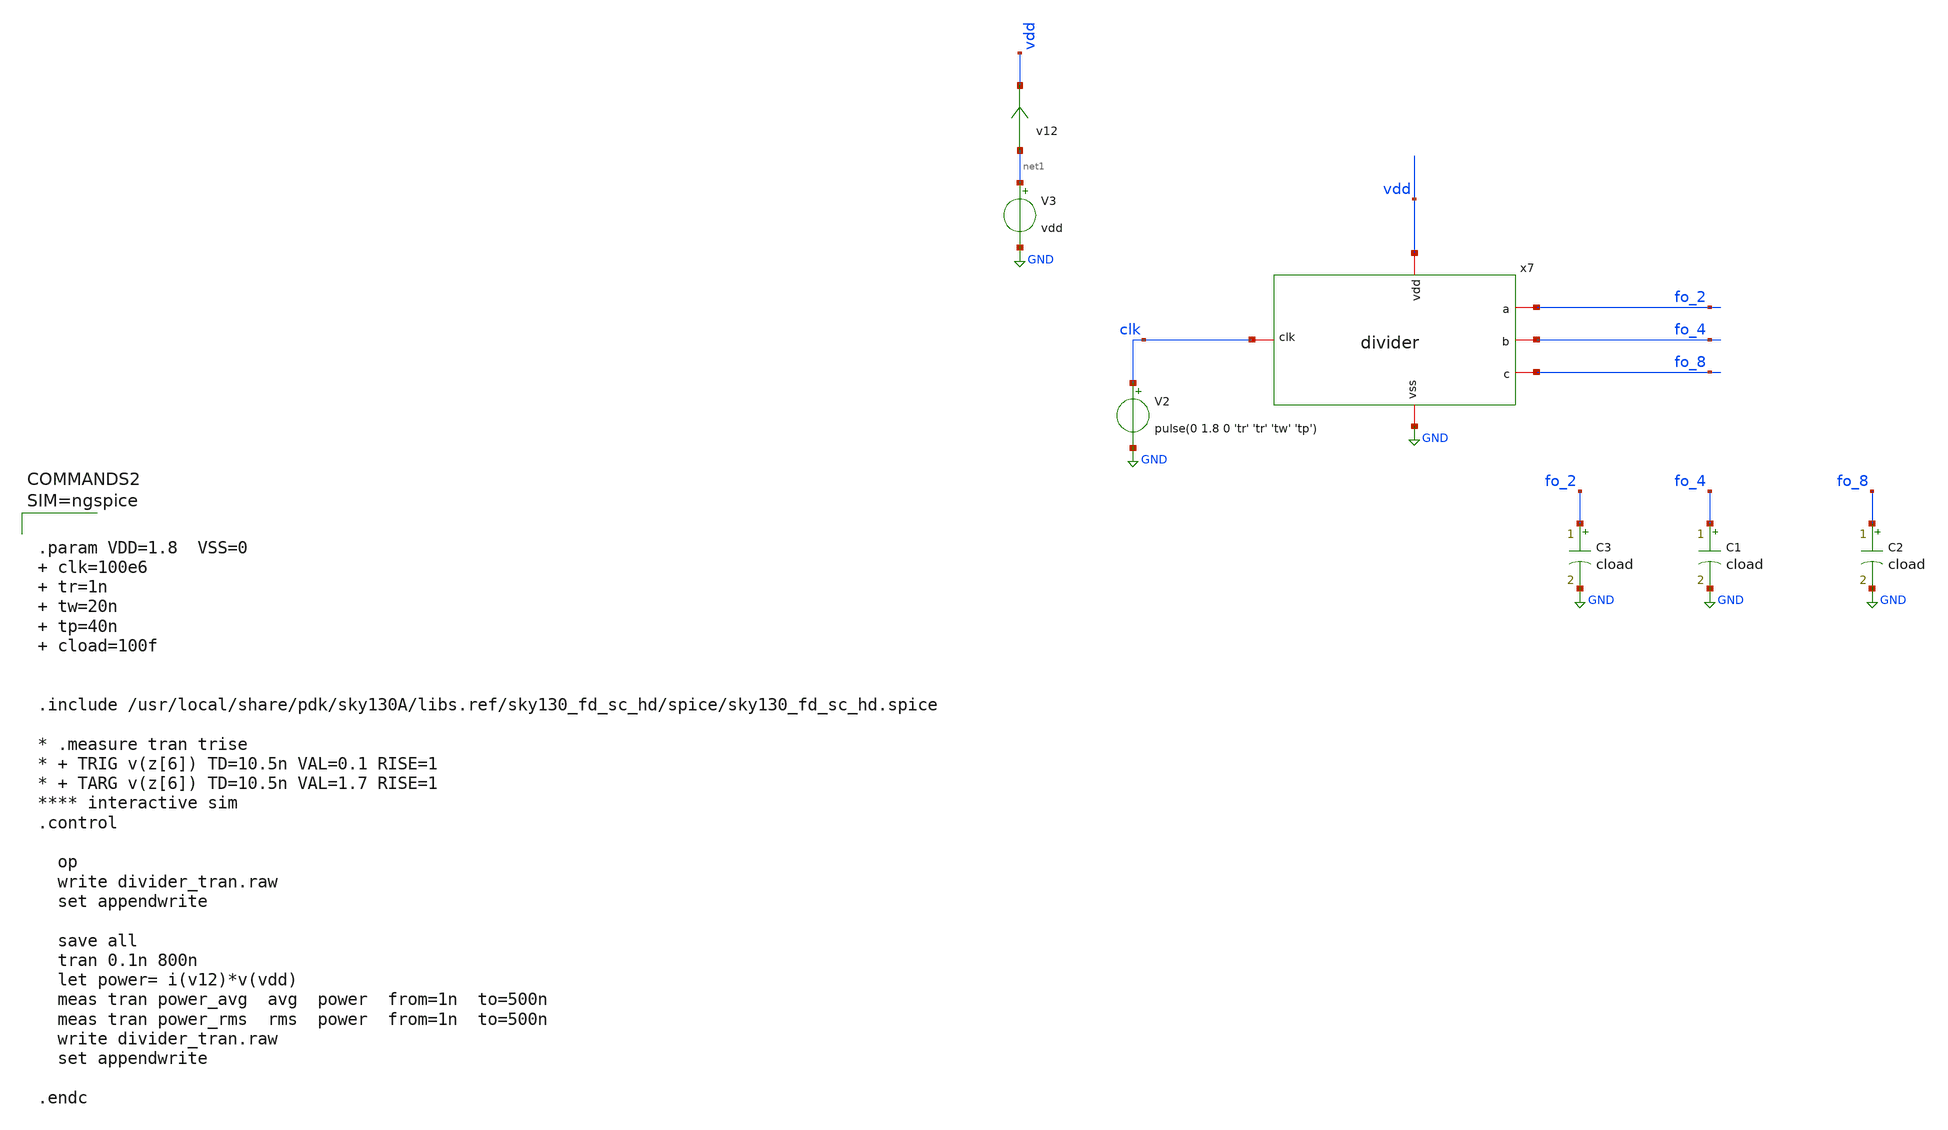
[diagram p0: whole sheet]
** sch_path: xschem/divider/divider_tran.sch
.lib $::SKYWATER_MODELS/sky130.lib.spice tt
.include $::SKYWATER_STDCELLS/sky130_fd_sc_hd.spice

**.subckt divider_tran
x7 fo_4 fo_8 fo_2 vdd GND clk divider
V3 net1 GND vdd
v12 net1 vdd 0
.save i(v12)
C3 fo_2 GND cload m=1
C1 fo_4 GND cload m=1
C2 fo_8 GND cload m=1
V2 clk GND pulse(0 1.8 0 'tr' 'tr' 'tw' 'tp')
**** begin user architecture code



.param VDD=1.8  VSS=0    clk=100e6  tr=1n  tw=20n  tp=40n   cload=100f


.include /usr/local/share/pdk/sky130A/libs.ref/sky130_fd_sc_hd/spice/sky130_fd_sc_hd.spice

* .measure tran trise
* + TRIG v(z[6]) TD=10.5n VAL=0.1 RISE=1
* + TARG v(z[6]) TD=10.5n VAL=1.7 RISE=1
**** interactive sim
.control

  op
  write divider_tran.raw
  set appendwrite

  save all
  tran 0.1n 800n
  let power= i(v12)*v(vdd)
  meas tran power_avg  avg  power  from=1n  to=500n
  meas tran power_rms  rms  power  from=1n  to=500n
  write divider_tran.raw
  set appendwrite

.endc



**** end user architecture code
**.ends

* expanding   symbol:  divider/divider.sym # of pins=6
** sym_path: xschem/divider/divider.sym
** sch_path: xschem/divider/divider.sch
.subckt divider b c a vdd vss clk
*.iopin clk
*.iopin vdd
*.iopin vss
*.iopin a
*.iopin b
*.iopin c
x3 clk net1 VSS VSS VDD VDD a net1 sky130_fd_sc_hd__dfxbp_2
x1 net1 net2 VSS VSS VDD VDD b net2 sky130_fd_sc_hd__dfxbp_2
x2 net2 net3 VSS VSS VDD VDD c net3 sky130_fd_sc_hd__dfxbp_2
.ends

.GLOBAL GND
.end
